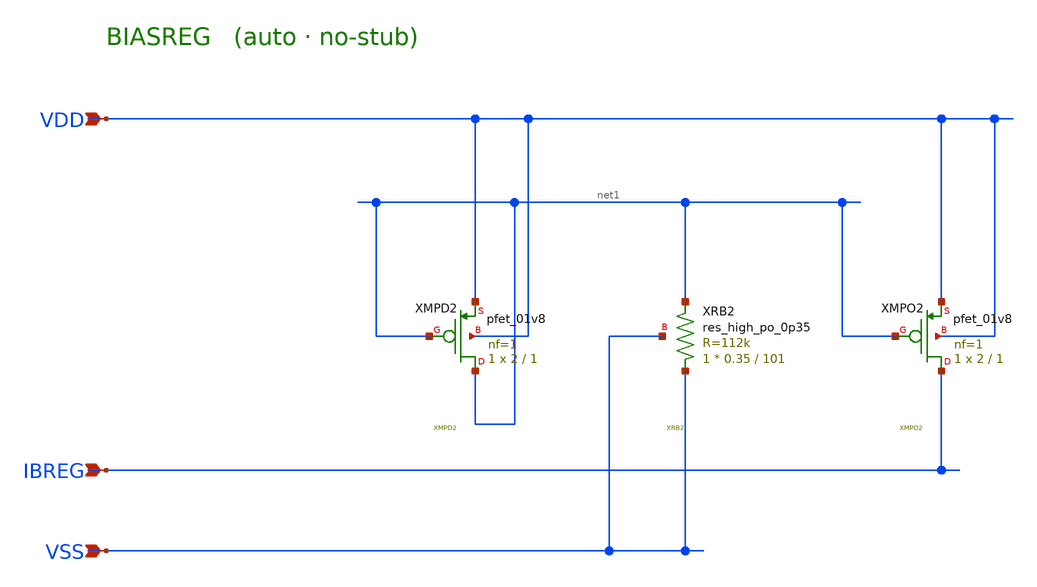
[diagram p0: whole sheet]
** sch_path: schematics/BIASREG.sch
**.subckt BIASREG VDD VSS IBREG
*.ipin VDD
*.ipin VSS
*.ipin IBREG
XXMPD2 net1 net1 VDD VDD sky130_fd_pr__pfet_01v8 L=1 W=2 nf=1 ad='int((nf+1)/2) * W/nf * 0.29' as='int((nf+2)/2) * W/nf * 0.29'
+ pd='2*int((nf+1)/2) * (W/nf + 0.29)' ps='2*int((nf+2)/2) * (W/nf + 0.29)' nrd='0.29 / W' nrs='0.29 / W'
+ sa=0 sb=0 sd=0 mult=1 m=1
XXRB2 VSS net1 VSS sky130_fd_pr__res_high_po_0p35 L=101 mult=1 m=1
XXMPO2 IBREG net1 VDD VDD sky130_fd_pr__pfet_01v8 L=1 W=2 nf=1 ad='int((nf+1)/2) * W/nf * 0.29' as='int((nf+2)/2) * W/nf * 0.29'
+ pd='2*int((nf+1)/2) * (W/nf + 0.29)' ps='2*int((nf+2)/2) * (W/nf + 0.29)' nrd='0.29 / W' nrs='0.29 / W'
+ sa=0 sb=0 sd=0 mult=1 m=1
**.ends
.end
